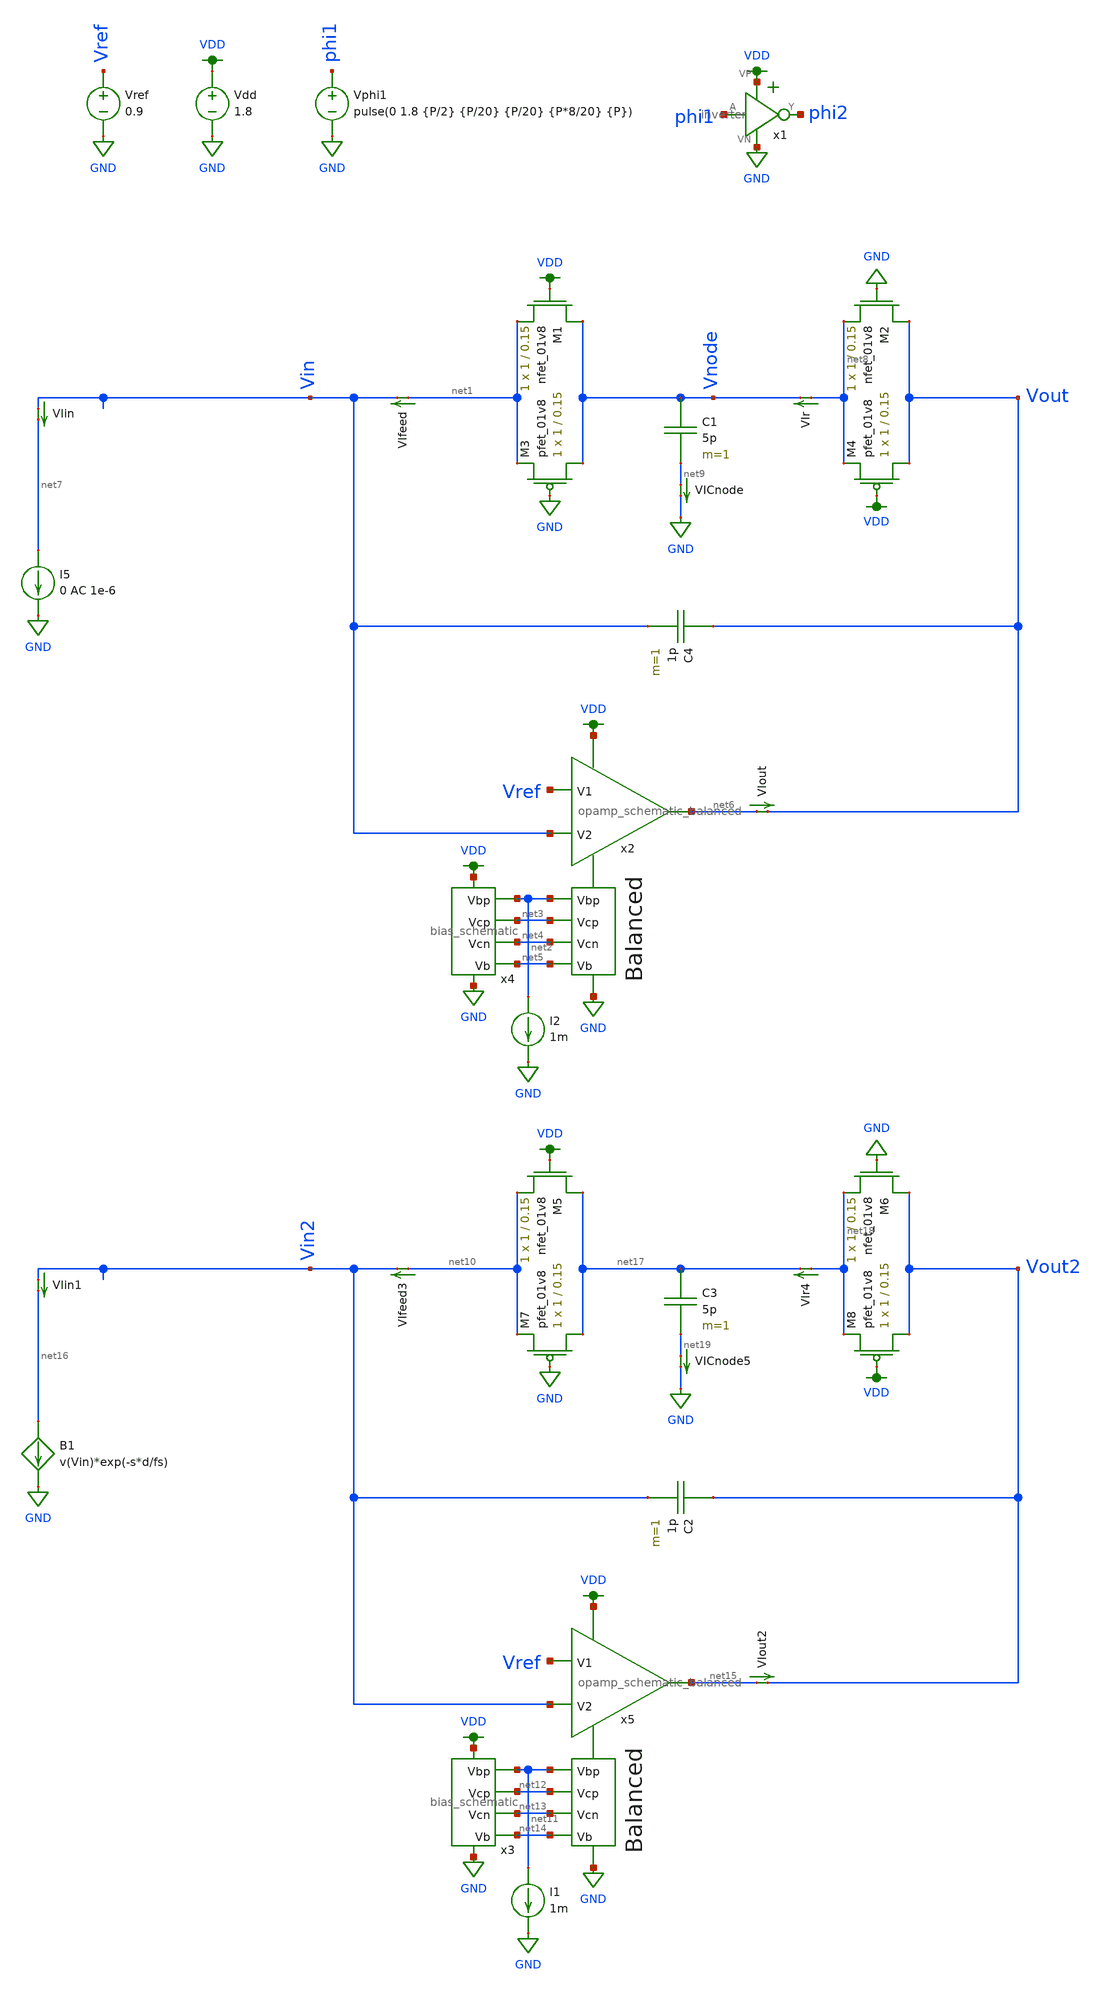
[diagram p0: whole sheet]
** sch_path: xschem/switched_capacitor/switched_capacitor_iv_bode_2_part.sch
**.subckt switched_capacitor_iv_bode_2_part
Vdd VDD GND 1.8
x4 VDD net2 net3 net4 GND net5 bias_schematic
Vref Vref GND 0.9
I2 net2 GND 1m
VIin Vin net7 0
.save i(viin)
VIout net6 Vout 0
.save i(viout)
VIfeed net1 Vin 0
.save i(vifeed)
C4 Vout Vin 1p m=1
x2 VDD net2 net3 net6 Vref Vin net4 net5 GND opamp_schematic_balanced
I5 net7 GND 0 AC 1e-6
C1 Vnode net9 5p m=1
XM1 Vnode VDD net1 GND sky130_fd_pr__nfet_01v8 L=0.15 W=1 nf=1 ad='int((nf+1)/2) * W/nf * 0.29' as='int((nf+2)/2) * W/nf * 0.29'
+ pd='2*int((nf+1)/2) * (W/nf + 0.29)' ps='2*int((nf+2)/2) * (W/nf + 0.29)' nrd='0.29 / W' nrs='0.29 / W'
+ sa=0 sb=0 sd=0 mult=1 m=1
XM2 Vout GND net8 GND sky130_fd_pr__nfet_01v8 L=0.15 W=1 nf=1 ad='int((nf+1)/2) * W/nf * 0.29' as='int((nf+2)/2) * W/nf * 0.29'
+ pd='2*int((nf+1)/2) * (W/nf + 0.29)' ps='2*int((nf+2)/2) * (W/nf + 0.29)' nrd='0.29 / W' nrs='0.29 / W'
+ sa=0 sb=0 sd=0 mult=1 m=1
XM3 Vnode GND net1 VDD sky130_fd_pr__pfet_01v8 L=0.15 W=1 nf=1 ad='int((nf+1)/2) * W/nf * 0.29' as='int((nf+2)/2) * W/nf * 0.29'
+ pd='2*int((nf+1)/2) * (W/nf + 0.29)' ps='2*int((nf+2)/2) * (W/nf + 0.29)' nrd='0.29 / W' nrs='0.29 / W'
+ sa=0 sb=0 sd=0 mult=1 m=1
XM4 Vout VDD net8 VDD sky130_fd_pr__pfet_01v8 L=0.15 W=1 nf=1 ad='int((nf+1)/2) * W/nf * 0.29' as='int((nf+2)/2) * W/nf * 0.29'
+ pd='2*int((nf+1)/2) * (W/nf + 0.29)' ps='2*int((nf+2)/2) * (W/nf + 0.29)' nrd='0.29 / W' nrs='0.29 / W'
+ sa=0 sb=0 sd=0 mult=1 m=1
x1 VDD phi1 phi2 GND inverter
VIr net8 Vnode 0
.save i(vir)
VICnode net9 GND 0
.save i(vicnode)
Vphi1 phi1 GND pulse(0 1.8 {P/2} {P/20} {P/20} {P*8/20} {P})
x3 VDD net11 net12 net13 GND net14 bias_schematic
I1 net11 GND 1m
VIin1 Vin2 net16 0
.save i(viin1)
VIout2 net15 Vout2 0
.save i(viout2)
VIfeed3 net10 Vin2 0
.save i(vifeed3)
C2 Vout2 Vin2 1p m=1
x5 VDD net11 net12 net15 Vref Vin2 net13 net14 GND opamp_schematic_balanced
C3 net17 net19 5p m=1
XM5 net17 VDD net10 GND sky130_fd_pr__nfet_01v8 L=0.15 W=1 nf=1 ad='int((nf+1)/2) * W/nf * 0.29' as='int((nf+2)/2) * W/nf * 0.29'
+ pd='2*int((nf+1)/2) * (W/nf + 0.29)' ps='2*int((nf+2)/2) * (W/nf + 0.29)' nrd='0.29 / W' nrs='0.29 / W'
+ sa=0 sb=0 sd=0 mult=1 m=1
XM6 Vout2 GND net18 GND sky130_fd_pr__nfet_01v8 L=0.15 W=1 nf=1 ad='int((nf+1)/2) * W/nf * 0.29' as='int((nf+2)/2) * W/nf * 0.29'
+ pd='2*int((nf+1)/2) * (W/nf + 0.29)' ps='2*int((nf+2)/2) * (W/nf + 0.29)' nrd='0.29 / W' nrs='0.29 / W'
+ sa=0 sb=0 sd=0 mult=1 m=1
XM7 net17 GND net10 VDD sky130_fd_pr__pfet_01v8 L=0.15 W=1 nf=1 ad='int((nf+1)/2) * W/nf * 0.29' as='int((nf+2)/2) * W/nf * 0.29'
+ pd='2*int((nf+1)/2) * (W/nf + 0.29)' ps='2*int((nf+2)/2) * (W/nf + 0.29)' nrd='0.29 / W' nrs='0.29 / W'
+ sa=0 sb=0 sd=0 mult=1 m=1
XM8 Vout2 VDD net18 VDD sky130_fd_pr__pfet_01v8 L=0.15 W=1 nf=1 ad='int((nf+1)/2) * W/nf * 0.29' as='int((nf+2)/2) * W/nf * 0.29'
+ pd='2*int((nf+1)/2) * (W/nf + 0.29)' ps='2*int((nf+2)/2) * (W/nf + 0.29)' nrd='0.29 / W' nrs='0.29 / W'
+ sa=0 sb=0 sd=0 mult=1 m=1
VIr4 net18 net17 0
.save i(vir4)
VICnode5 net19 GND 0
.save i(vicnode5)
B1 net16 GND I=v(Vin)*exp(-s*d/fs)
**** begin user architecture code

.option wnflag=1
.param MC_SWITCH=0.0
.lib ~/skywater/skywater-pdk/libraries/sky130_fd_pr_ngspice/latest/models/sky130.lib.spice tt


.param P=10n
.pss 5e-6 Vout 1024 50
.param fs=100Meg d=0.5
ac dec 1e2 1 1e10
*.control
*save all
*ac dec 1e-1 1 1e10
*run
*plot db(v(Vout)) cph(v(Vout))*180/pi
*.endc

**** end user architecture code
**.ends

* expanding   symbol:  /home/madvlsi/dev/git/magic-dds/xschem/other_project_files/bias_schematic.sym
*+ # of pins=6
** sym_path: xschem/other_project_files/bias_schematic.sym
** sch_path: xschem/other_project_files/bias_schematic.sch
.subckt bias_schematic VP Vbp Vcp Vcn VN Vb
*.iopin VP
*.iopin VN
*.opin Vcp
*.iopin Vbp
*.opin Vcn
*.opin Vb
XM1a net2 net2 net1 GND sky130_fd_pr__nfet_01v8 L=0.5 W=3 nf=1 ad='int((nf+1)/2) * W/nf * 0.29' as='int((nf+2)/2) * W/nf * 0.29'
+ pd='2*int((nf+1)/2) * (W/nf + 0.29)' ps='2*int((nf+2)/2) * (W/nf + 0.29)' nrd='0.29 / W' nrs='0.29 / W'
+ sa=0 sb=0 sd=0 mult=1 m=1
XM1b net2 net2 net1 GND sky130_fd_pr__nfet_01v8 L=0.5 W=3 nf=1 ad='int((nf+1)/2) * W/nf * 0.29' as='int((nf+2)/2) * W/nf * 0.29'
+ pd='2*int((nf+1)/2) * (W/nf + 0.29)' ps='2*int((nf+2)/2) * (W/nf + 0.29)' nrd='0.29 / W' nrs='0.29 / W'
+ sa=0 sb=0 sd=0 mult=1 m=1
XM1c net2 net2 net1 GND sky130_fd_pr__nfet_01v8 L=0.5 W=3 nf=1 ad='int((nf+1)/2) * W/nf * 0.29' as='int((nf+2)/2) * W/nf * 0.29'
+ pd='2*int((nf+1)/2) * (W/nf + 0.29)' ps='2*int((nf+2)/2) * (W/nf + 0.29)' nrd='0.29 / W' nrs='0.29 / W'
+ sa=0 sb=0 sd=0 mult=1 m=1
XM1d net2 net2 net1 GND sky130_fd_pr__nfet_01v8 L=0.5 W=3 nf=1 ad='int((nf+1)/2) * W/nf * 0.29' as='int((nf+2)/2) * W/nf * 0.29'
+ pd='2*int((nf+1)/2) * (W/nf + 0.29)' ps='2*int((nf+2)/2) * (W/nf + 0.29)' nrd='0.29 / W' nrs='0.29 / W'
+ sa=0 sb=0 sd=0 mult=1 m=1
XM2a VN net2 net1 GND sky130_fd_pr__nfet_01v8 L=0.5 W=3 nf=1 ad='int((nf+1)/2) * W/nf * 0.29' as='int((nf+2)/2) * W/nf * 0.29'
+ pd='2*int((nf+1)/2) * (W/nf + 0.29)' ps='2*int((nf+2)/2) * (W/nf + 0.29)' nrd='0.29 / W' nrs='0.29 / W'
+ sa=0 sb=0 sd=0 mult=1 m=1
XM2b VN net2 net1 GND sky130_fd_pr__nfet_01v8 L=0.5 W=3 nf=1 ad='int((nf+1)/2) * W/nf * 0.29' as='int((nf+2)/2) * W/nf * 0.29'
+ pd='2*int((nf+1)/2) * (W/nf + 0.29)' ps='2*int((nf+2)/2) * (W/nf + 0.29)' nrd='0.29 / W' nrs='0.29 / W'
+ sa=0 sb=0 sd=0 mult=1 m=1
XM2c VN net2 net1 GND sky130_fd_pr__nfet_01v8 L=0.5 W=3 nf=1 ad='int((nf+1)/2) * W/nf * 0.29' as='int((nf+2)/2) * W/nf * 0.29'
+ pd='2*int((nf+1)/2) * (W/nf + 0.29)' ps='2*int((nf+2)/2) * (W/nf + 0.29)' nrd='0.29 / W' nrs='0.29 / W'
+ sa=0 sb=0 sd=0 mult=1 m=1
XM2d VN net2 net1 GND sky130_fd_pr__nfet_01v8 L=0.5 W=3 nf=1 ad='int((nf+1)/2) * W/nf * 0.29' as='int((nf+2)/2) * W/nf * 0.29'
+ pd='2*int((nf+1)/2) * (W/nf + 0.29)' ps='2*int((nf+2)/2) * (W/nf + 0.29)' nrd='0.29 / W' nrs='0.29 / W'
+ sa=0 sb=0 sd=0 mult=1 m=1
XM3a net2 Vbp net7 VDD sky130_fd_pr__pfet_01v8 L=0.5 W=3 nf=1 ad='int((nf+1)/2) * W/nf * 0.29' as='int((nf+2)/2) * W/nf * 0.29'
+ pd='2*int((nf+1)/2) * (W/nf + 0.29)' ps='2*int((nf+2)/2) * (W/nf + 0.29)' nrd='0.29 / W' nrs='0.29 / W'
+ sa=0 sb=0 sd=0 mult=1 m=1
XM3b net7 Vbp net6 VDD sky130_fd_pr__pfet_01v8 L=0.5 W=3 nf=1 ad='int((nf+1)/2) * W/nf * 0.29' as='int((nf+2)/2) * W/nf * 0.29'
+ pd='2*int((nf+1)/2) * (W/nf + 0.29)' ps='2*int((nf+2)/2) * (W/nf + 0.29)' nrd='0.29 / W' nrs='0.29 / W'
+ sa=0 sb=0 sd=0 mult=1 m=1
XM3c net6 Vbp net5 VDD sky130_fd_pr__pfet_01v8 L=0.5 W=3 nf=1 ad='int((nf+1)/2) * W/nf * 0.29' as='int((nf+2)/2) * W/nf * 0.29'
+ pd='2*int((nf+1)/2) * (W/nf + 0.29)' ps='2*int((nf+2)/2) * (W/nf + 0.29)' nrd='0.29 / W' nrs='0.29 / W'
+ sa=0 sb=0 sd=0 mult=1 m=1
XM3d net5 Vbp VP VDD sky130_fd_pr__pfet_01v8 L=0.5 W=3 nf=1 ad='int((nf+1)/2) * W/nf * 0.29' as='int((nf+2)/2) * W/nf * 0.29'
+ pd='2*int((nf+1)/2) * (W/nf + 0.29)' ps='2*int((nf+2)/2) * (W/nf + 0.29)' nrd='0.29 / W' nrs='0.29 / W'
+ sa=0 sb=0 sd=0 mult=1 m=1
XM4a Vcn Vbp VP VDD sky130_fd_pr__pfet_01v8 L=0.5 W=3 nf=1 ad='int((nf+1)/2) * W/nf * 0.29' as='int((nf+2)/2) * W/nf * 0.29'
+ pd='2*int((nf+1)/2) * (W/nf + 0.29)' ps='2*int((nf+2)/2) * (W/nf + 0.29)' nrd='0.29 / W' nrs='0.29 / W'
+ sa=0 sb=0 sd=0 mult=1 m=1
XM4b Vcn Vbp VP VDD sky130_fd_pr__pfet_01v8 L=0.5 W=3 nf=1 ad='int((nf+1)/2) * W/nf * 0.29' as='int((nf+2)/2) * W/nf * 0.29'
+ pd='2*int((nf+1)/2) * (W/nf + 0.29)' ps='2*int((nf+2)/2) * (W/nf + 0.29)' nrd='0.29 / W' nrs='0.29 / W'
+ sa=0 sb=0 sd=0 mult=1 m=1
XM4c Vcn Vbp VP VDD sky130_fd_pr__pfet_01v8 L=0.5 W=3 nf=1 ad='int((nf+1)/2) * W/nf * 0.29' as='int((nf+2)/2) * W/nf * 0.29'
+ pd='2*int((nf+1)/2) * (W/nf + 0.29)' ps='2*int((nf+2)/2) * (W/nf + 0.29)' nrd='0.29 / W' nrs='0.29 / W'
+ sa=0 sb=0 sd=0 mult=1 m=1
XM4d Vcn Vbp VP VDD sky130_fd_pr__pfet_01v8 L=0.5 W=3 nf=1 ad='int((nf+1)/2) * W/nf * 0.29' as='int((nf+2)/2) * W/nf * 0.29'
+ pd='2*int((nf+1)/2) * (W/nf + 0.29)' ps='2*int((nf+2)/2) * (W/nf + 0.29)' nrd='0.29 / W' nrs='0.29 / W'
+ sa=0 sb=0 sd=0 mult=1 m=1
XM11a VP Vbp Vbp VDD sky130_fd_pr__pfet_01v8 L=0.5 W=3 nf=1 ad='int((nf+1)/2) * W/nf * 0.29' as='int((nf+2)/2) * W/nf * 0.29'
+ pd='2*int((nf+1)/2) * (W/nf + 0.29)' ps='2*int((nf+2)/2) * (W/nf + 0.29)' nrd='0.29 / W' nrs='0.29 / W'
+ sa=0 sb=0 sd=0 mult=1 m=1
XM11b VP Vbp Vbp VDD sky130_fd_pr__pfet_01v8 L=0.5 W=3 nf=1 ad='int((nf+1)/2) * W/nf * 0.29' as='int((nf+2)/2) * W/nf * 0.29'
+ pd='2*int((nf+1)/2) * (W/nf + 0.29)' ps='2*int((nf+2)/2) * (W/nf + 0.29)' nrd='0.29 / W' nrs='0.29 / W'
+ sa=0 sb=0 sd=0 mult=1 m=1
XM11c VP Vbp Vbp VDD sky130_fd_pr__pfet_01v8 L=0.5 W=3 nf=1 ad='int((nf+1)/2) * W/nf * 0.29' as='int((nf+2)/2) * W/nf * 0.29'
+ pd='2*int((nf+1)/2) * (W/nf + 0.29)' ps='2*int((nf+2)/2) * (W/nf + 0.29)' nrd='0.29 / W' nrs='0.29 / W'
+ sa=0 sb=0 sd=0 mult=1 m=1
XM11d VP Vbp Vbp VDD sky130_fd_pr__pfet_01v8 L=0.5 W=3 nf=1 ad='int((nf+1)/2) * W/nf * 0.29' as='int((nf+2)/2) * W/nf * 0.29'
+ pd='2*int((nf+1)/2) * (W/nf + 0.29)' ps='2*int((nf+2)/2) * (W/nf + 0.29)' nrd='0.29 / W' nrs='0.29 / W'
+ sa=0 sb=0 sd=0 mult=1 m=1
XM5a net1 Vcn Vcn GND sky130_fd_pr__nfet_01v8 L=0.5 W=3 nf=1 ad='int((nf+1)/2) * W/nf * 0.29' as='int((nf+2)/2) * W/nf * 0.29'
+ pd='2*int((nf+1)/2) * (W/nf + 0.29)' ps='2*int((nf+2)/2) * (W/nf + 0.29)' nrd='0.29 / W' nrs='0.29 / W'
+ sa=0 sb=0 sd=0 mult=1 m=1
XM5b net1 Vcn Vcn GND sky130_fd_pr__nfet_01v8 L=0.5 W=3 nf=1 ad='int((nf+1)/2) * W/nf * 0.29' as='int((nf+2)/2) * W/nf * 0.29'
+ pd='2*int((nf+1)/2) * (W/nf + 0.29)' ps='2*int((nf+2)/2) * (W/nf + 0.29)' nrd='0.29 / W' nrs='0.29 / W'
+ sa=0 sb=0 sd=0 mult=1 m=1
XM5c net1 Vcn Vcn GND sky130_fd_pr__nfet_01v8 L=0.5 W=3 nf=1 ad='int((nf+1)/2) * W/nf * 0.29' as='int((nf+2)/2) * W/nf * 0.29'
+ pd='2*int((nf+1)/2) * (W/nf + 0.29)' ps='2*int((nf+2)/2) * (W/nf + 0.29)' nrd='0.29 / W' nrs='0.29 / W'
+ sa=0 sb=0 sd=0 mult=1 m=1
XM5d net1 Vcn Vcn GND sky130_fd_pr__nfet_01v8 L=0.5 W=3 nf=1 ad='int((nf+1)/2) * W/nf * 0.29' as='int((nf+2)/2) * W/nf * 0.29'
+ pd='2*int((nf+1)/2) * (W/nf + 0.29)' ps='2*int((nf+2)/2) * (W/nf + 0.29)' nrd='0.29 / W' nrs='0.29 / W'
+ sa=0 sb=0 sd=0 mult=1 m=1
XM8a net10 Vb net3 GND sky130_fd_pr__nfet_01v8 L=0.5 W=3 nf=1 ad='int((nf+1)/2) * W/nf * 0.29' as='int((nf+2)/2) * W/nf * 0.29'
+ pd='2*int((nf+1)/2) * (W/nf + 0.29)' ps='2*int((nf+2)/2) * (W/nf + 0.29)' nrd='0.29 / W' nrs='0.29 / W'
+ sa=0 sb=0 sd=0 mult=1 m=1
XM8b net9 Vb net10 GND sky130_fd_pr__nfet_01v8 L=0.5 W=3 nf=1 ad='int((nf+1)/2) * W/nf * 0.29' as='int((nf+2)/2) * W/nf * 0.29'
+ pd='2*int((nf+1)/2) * (W/nf + 0.29)' ps='2*int((nf+2)/2) * (W/nf + 0.29)' nrd='0.29 / W' nrs='0.29 / W'
+ sa=0 sb=0 sd=0 mult=1 m=1
XM8c net8 Vb net9 GND sky130_fd_pr__nfet_01v8 L=0.5 W=3 nf=1 ad='int((nf+1)/2) * W/nf * 0.29' as='int((nf+2)/2) * W/nf * 0.29'
+ pd='2*int((nf+1)/2) * (W/nf + 0.29)' ps='2*int((nf+2)/2) * (W/nf + 0.29)' nrd='0.29 / W' nrs='0.29 / W'
+ sa=0 sb=0 sd=0 mult=1 m=1
XM8d VN Vb net8 GND sky130_fd_pr__nfet_01v8 L=0.5 W=3 nf=1 ad='int((nf+1)/2) * W/nf * 0.29' as='int((nf+2)/2) * W/nf * 0.29'
+ pd='2*int((nf+1)/2) * (W/nf + 0.29)' ps='2*int((nf+2)/2) * (W/nf + 0.29)' nrd='0.29 / W' nrs='0.29 / W'
+ sa=0 sb=0 sd=0 mult=1 m=1
XM6a net3 net3 net4 VDD sky130_fd_pr__pfet_01v8 L=0.5 W=3 nf=1 ad='int((nf+1)/2) * W/nf * 0.29' as='int((nf+2)/2) * W/nf * 0.29'
+ pd='2*int((nf+1)/2) * (W/nf + 0.29)' ps='2*int((nf+2)/2) * (W/nf + 0.29)' nrd='0.29 / W' nrs='0.29 / W'
+ sa=0 sb=0 sd=0 mult=1 m=1
XM6b net3 net3 net4 VDD sky130_fd_pr__pfet_01v8 L=0.5 W=3 nf=1 ad='int((nf+1)/2) * W/nf * 0.29' as='int((nf+2)/2) * W/nf * 0.29'
+ pd='2*int((nf+1)/2) * (W/nf + 0.29)' ps='2*int((nf+2)/2) * (W/nf + 0.29)' nrd='0.29 / W' nrs='0.29 / W'
+ sa=0 sb=0 sd=0 mult=1 m=1
XM6c net3 net3 net4 VDD sky130_fd_pr__pfet_01v8 L=0.5 W=3 nf=1 ad='int((nf+1)/2) * W/nf * 0.29' as='int((nf+2)/2) * W/nf * 0.29'
+ pd='2*int((nf+1)/2) * (W/nf + 0.29)' ps='2*int((nf+2)/2) * (W/nf + 0.29)' nrd='0.29 / W' nrs='0.29 / W'
+ sa=0 sb=0 sd=0 mult=1 m=1
XM6d net3 net3 net4 VDD sky130_fd_pr__pfet_01v8 L=0.5 W=3 nf=1 ad='int((nf+1)/2) * W/nf * 0.29' as='int((nf+2)/2) * W/nf * 0.29'
+ pd='2*int((nf+1)/2) * (W/nf + 0.29)' ps='2*int((nf+2)/2) * (W/nf + 0.29)' nrd='0.29 / W' nrs='0.29 / W'
+ sa=0 sb=0 sd=0 mult=1 m=1
XM7a net4 net3 VP VDD sky130_fd_pr__pfet_01v8 L=0.5 W=3 nf=1 ad='int((nf+1)/2) * W/nf * 0.29' as='int((nf+2)/2) * W/nf * 0.29'
+ pd='2*int((nf+1)/2) * (W/nf + 0.29)' ps='2*int((nf+2)/2) * (W/nf + 0.29)' nrd='0.29 / W' nrs='0.29 / W'
+ sa=0 sb=0 sd=0 mult=1 m=1
XM7b net4 net3 VP VDD sky130_fd_pr__pfet_01v8 L=0.5 W=3 nf=1 ad='int((nf+1)/2) * W/nf * 0.29' as='int((nf+2)/2) * W/nf * 0.29'
+ pd='2*int((nf+1)/2) * (W/nf + 0.29)' ps='2*int((nf+2)/2) * (W/nf + 0.29)' nrd='0.29 / W' nrs='0.29 / W'
+ sa=0 sb=0 sd=0 mult=1 m=1
XM7c net4 net3 VP VDD sky130_fd_pr__pfet_01v8 L=0.5 W=3 nf=1 ad='int((nf+1)/2) * W/nf * 0.29' as='int((nf+2)/2) * W/nf * 0.29'
+ pd='2*int((nf+1)/2) * (W/nf + 0.29)' ps='2*int((nf+2)/2) * (W/nf + 0.29)' nrd='0.29 / W' nrs='0.29 / W'
+ sa=0 sb=0 sd=0 mult=1 m=1
XM7d net4 net3 VP VDD sky130_fd_pr__pfet_01v8 L=0.5 W=3 nf=1 ad='int((nf+1)/2) * W/nf * 0.29' as='int((nf+2)/2) * W/nf * 0.29'
+ pd='2*int((nf+1)/2) * (W/nf + 0.29)' ps='2*int((nf+2)/2) * (W/nf + 0.29)' nrd='0.29 / W' nrs='0.29 / W'
+ sa=0 sb=0 sd=0 mult=1 m=1
XM10d net4 Vcp Vcp VDD sky130_fd_pr__pfet_01v8 L=0.5 W=3 nf=1 ad='int((nf+1)/2) * W/nf * 0.29' as='int((nf+2)/2) * W/nf * 0.29'
+ pd='2*int((nf+1)/2) * (W/nf + 0.29)' ps='2*int((nf+2)/2) * (W/nf + 0.29)' nrd='0.29 / W' nrs='0.29 / W'
+ sa=0 sb=0 sd=0 mult=1 m=1
XM10c net4 Vcp Vcp VDD sky130_fd_pr__pfet_01v8 L=0.5 W=3 nf=1 ad='int((nf+1)/2) * W/nf * 0.29' as='int((nf+2)/2) * W/nf * 0.29'
+ pd='2*int((nf+1)/2) * (W/nf + 0.29)' ps='2*int((nf+2)/2) * (W/nf + 0.29)' nrd='0.29 / W' nrs='0.29 / W'
+ sa=0 sb=0 sd=0 mult=1 m=1
XM10b net4 Vcp Vcp VDD sky130_fd_pr__pfet_01v8 L=0.5 W=3 nf=1 ad='int((nf+1)/2) * W/nf * 0.29' as='int((nf+2)/2) * W/nf * 0.29'
+ pd='2*int((nf+1)/2) * (W/nf + 0.29)' ps='2*int((nf+2)/2) * (W/nf + 0.29)' nrd='0.29 / W' nrs='0.29 / W'
+ sa=0 sb=0 sd=0 mult=1 m=1
XM10a net4 Vcp Vcp VDD sky130_fd_pr__pfet_01v8 L=0.5 W=3 nf=1 ad='int((nf+1)/2) * W/nf * 0.29' as='int((nf+2)/2) * W/nf * 0.29'
+ pd='2*int((nf+1)/2) * (W/nf + 0.29)' ps='2*int((nf+2)/2) * (W/nf + 0.29)' nrd='0.29 / W' nrs='0.29 / W'
+ sa=0 sb=0 sd=0 mult=1 m=1
XM9a VN Vb Vcp GND sky130_fd_pr__nfet_01v8 L=0.5 W=3 nf=1 ad='int((nf+1)/2) * W/nf * 0.29' as='int((nf+2)/2) * W/nf * 0.29'
+ pd='2*int((nf+1)/2) * (W/nf + 0.29)' ps='2*int((nf+2)/2) * (W/nf + 0.29)' nrd='0.29 / W' nrs='0.29 / W'
+ sa=0 sb=0 sd=0 mult=1 m=1
XM9b VN Vb Vcp GND sky130_fd_pr__nfet_01v8 L=0.5 W=3 nf=1 ad='int((nf+1)/2) * W/nf * 0.29' as='int((nf+2)/2) * W/nf * 0.29'
+ pd='2*int((nf+1)/2) * (W/nf + 0.29)' ps='2*int((nf+2)/2) * (W/nf + 0.29)' nrd='0.29 / W' nrs='0.29 / W'
+ sa=0 sb=0 sd=0 mult=1 m=1
XM9c VN Vb Vcp GND sky130_fd_pr__nfet_01v8 L=0.5 W=3 nf=1 ad='int((nf+1)/2) * W/nf * 0.29' as='int((nf+2)/2) * W/nf * 0.29'
+ pd='2*int((nf+1)/2) * (W/nf + 0.29)' ps='2*int((nf+2)/2) * (W/nf + 0.29)' nrd='0.29 / W' nrs='0.29 / W'
+ sa=0 sb=0 sd=0 mult=1 m=1
XM9d VN Vb Vcp GND sky130_fd_pr__nfet_01v8 L=0.5 W=3 nf=1 ad='int((nf+1)/2) * W/nf * 0.29' as='int((nf+2)/2) * W/nf * 0.29'
+ pd='2*int((nf+1)/2) * (W/nf + 0.29)' ps='2*int((nf+2)/2) * (W/nf + 0.29)' nrd='0.29 / W' nrs='0.29 / W'
+ sa=0 sb=0 sd=0 mult=1 m=1
XM12a VN Vb Vb GND sky130_fd_pr__nfet_01v8 L=0.5 W=3 nf=1 ad='int((nf+1)/2) * W/nf * 0.29' as='int((nf+2)/2) * W/nf * 0.29'
+ pd='2*int((nf+1)/2) * (W/nf + 0.29)' ps='2*int((nf+2)/2) * (W/nf + 0.29)' nrd='0.29 / W' nrs='0.29 / W'
+ sa=0 sb=0 sd=0 mult=1 m=1
XM12b VN Vb Vb GND sky130_fd_pr__nfet_01v8 L=0.5 W=3 nf=1 ad='int((nf+1)/2) * W/nf * 0.29' as='int((nf+2)/2) * W/nf * 0.29'
+ pd='2*int((nf+1)/2) * (W/nf + 0.29)' ps='2*int((nf+2)/2) * (W/nf + 0.29)' nrd='0.29 / W' nrs='0.29 / W'
+ sa=0 sb=0 sd=0 mult=1 m=1
XM12c VN Vb Vb GND sky130_fd_pr__nfet_01v8 L=0.5 W=3 nf=1 ad='int((nf+1)/2) * W/nf * 0.29' as='int((nf+2)/2) * W/nf * 0.29'
+ pd='2*int((nf+1)/2) * (W/nf + 0.29)' ps='2*int((nf+2)/2) * (W/nf + 0.29)' nrd='0.29 / W' nrs='0.29 / W'
+ sa=0 sb=0 sd=0 mult=1 m=1
XM12d VN Vb Vb GND sky130_fd_pr__nfet_01v8 L=0.5 W=3 nf=1 ad='int((nf+1)/2) * W/nf * 0.29' as='int((nf+2)/2) * W/nf * 0.29'
+ pd='2*int((nf+1)/2) * (W/nf + 0.29)' ps='2*int((nf+2)/2) * (W/nf + 0.29)' nrd='0.29 / W' nrs='0.29 / W'
+ sa=0 sb=0 sd=0 mult=1 m=1
XM1 Vb Vbp VP VDD sky130_fd_pr__pfet_01v8 L=0.5 W=3 nf=1 ad='int((nf+1)/2) * W/nf * 0.29' as='int((nf+2)/2) * W/nf * 0.29'
+ pd='2*int((nf+1)/2) * (W/nf + 0.29)' ps='2*int((nf+2)/2) * (W/nf + 0.29)' nrd='0.29 / W' nrs='0.29 / W'
+ sa=0 sb=0 sd=0 mult=1 m=1
XM2 Vb Vbp VP VDD sky130_fd_pr__pfet_01v8 L=0.5 W=3 nf=1 ad='int((nf+1)/2) * W/nf * 0.29' as='int((nf+2)/2) * W/nf * 0.29'
+ pd='2*int((nf+1)/2) * (W/nf + 0.29)' ps='2*int((nf+2)/2) * (W/nf + 0.29)' nrd='0.29 / W' nrs='0.29 / W'
+ sa=0 sb=0 sd=0 mult=1 m=1
XM3 Vb Vbp VP VDD sky130_fd_pr__pfet_01v8 L=0.5 W=3 nf=1 ad='int((nf+1)/2) * W/nf * 0.29' as='int((nf+2)/2) * W/nf * 0.29'
+ pd='2*int((nf+1)/2) * (W/nf + 0.29)' ps='2*int((nf+2)/2) * (W/nf + 0.29)' nrd='0.29 / W' nrs='0.29 / W'
+ sa=0 sb=0 sd=0 mult=1 m=1
XM4 Vb Vbp VP VDD sky130_fd_pr__pfet_01v8 L=0.5 W=3 nf=1 ad='int((nf+1)/2) * W/nf * 0.29' as='int((nf+2)/2) * W/nf * 0.29'
+ pd='2*int((nf+1)/2) * (W/nf + 0.29)' ps='2*int((nf+2)/2) * (W/nf + 0.29)' nrd='0.29 / W' nrs='0.29 / W'
+ sa=0 sb=0 sd=0 mult=1 m=1
XM1e net2 net2 net1 GND sky130_fd_pr__nfet_01v8 L=0.5 W=3 nf=1 ad='int((nf+1)/2) * W/nf * 0.29' as='int((nf+2)/2) * W/nf * 0.29'
+ pd='2*int((nf+1)/2) * (W/nf + 0.29)' ps='2*int((nf+2)/2) * (W/nf + 0.29)' nrd='0.29 / W' nrs='0.29 / W'
+ sa=0 sb=0 sd=0 mult=1 m=1
XM1f net2 net2 net1 GND sky130_fd_pr__nfet_01v8 L=0.5 W=3 nf=1 ad='int((nf+1)/2) * W/nf * 0.29' as='int((nf+2)/2) * W/nf * 0.29'
+ pd='2*int((nf+1)/2) * (W/nf + 0.29)' ps='2*int((nf+2)/2) * (W/nf + 0.29)' nrd='0.29 / W' nrs='0.29 / W'
+ sa=0 sb=0 sd=0 mult=1 m=1
XM1g net2 net2 net1 GND sky130_fd_pr__nfet_01v8 L=0.5 W=3 nf=1 ad='int((nf+1)/2) * W/nf * 0.29' as='int((nf+2)/2) * W/nf * 0.29'
+ pd='2*int((nf+1)/2) * (W/nf + 0.29)' ps='2*int((nf+2)/2) * (W/nf + 0.29)' nrd='0.29 / W' nrs='0.29 / W'
+ sa=0 sb=0 sd=0 mult=1 m=1
XM1h net2 net2 net1 GND sky130_fd_pr__nfet_01v8 L=0.5 W=3 nf=1 ad='int((nf+1)/2) * W/nf * 0.29' as='int((nf+2)/2) * W/nf * 0.29'
+ pd='2*int((nf+1)/2) * (W/nf + 0.29)' ps='2*int((nf+2)/2) * (W/nf + 0.29)' nrd='0.29 / W' nrs='0.29 / W'
+ sa=0 sb=0 sd=0 mult=1 m=1
XM6e net3 net3 net4 VDD sky130_fd_pr__pfet_01v8 L=0.5 W=3 nf=1 ad='int((nf+1)/2) * W/nf * 0.29' as='int((nf+2)/2) * W/nf * 0.29'
+ pd='2*int((nf+1)/2) * (W/nf + 0.29)' ps='2*int((nf+2)/2) * (W/nf + 0.29)' nrd='0.29 / W' nrs='0.29 / W'
+ sa=0 sb=0 sd=0 mult=1 m=1
XM6f net3 net3 net4 VDD sky130_fd_pr__pfet_01v8 L=0.5 W=3 nf=1 ad='int((nf+1)/2) * W/nf * 0.29' as='int((nf+2)/2) * W/nf * 0.29'
+ pd='2*int((nf+1)/2) * (W/nf + 0.29)' ps='2*int((nf+2)/2) * (W/nf + 0.29)' nrd='0.29 / W' nrs='0.29 / W'
+ sa=0 sb=0 sd=0 mult=1 m=1
XM6g net3 net3 net4 VDD sky130_fd_pr__pfet_01v8 L=0.5 W=3 nf=1 ad='int((nf+1)/2) * W/nf * 0.29' as='int((nf+2)/2) * W/nf * 0.29'
+ pd='2*int((nf+1)/2) * (W/nf + 0.29)' ps='2*int((nf+2)/2) * (W/nf + 0.29)' nrd='0.29 / W' nrs='0.29 / W'
+ sa=0 sb=0 sd=0 mult=1 m=1
XM6h net3 net3 net4 VDD sky130_fd_pr__pfet_01v8 L=0.5 W=3 nf=1 ad='int((nf+1)/2) * W/nf * 0.29' as='int((nf+2)/2) * W/nf * 0.29'
+ pd='2*int((nf+1)/2) * (W/nf + 0.29)' ps='2*int((nf+2)/2) * (W/nf + 0.29)' nrd='0.29 / W' nrs='0.29 / W'
+ sa=0 sb=0 sd=0 mult=1 m=1
XM1i net2 net2 net1 GND sky130_fd_pr__nfet_01v8 L=0.5 W=3 nf=1 ad='int((nf+1)/2) * W/nf * 0.29' as='int((nf+2)/2) * W/nf * 0.29'
+ pd='2*int((nf+1)/2) * (W/nf + 0.29)' ps='2*int((nf+2)/2) * (W/nf + 0.29)' nrd='0.29 / W' nrs='0.29 / W'
+ sa=0 sb=0 sd=0 mult=1 m=1
XM1j net2 net2 net1 GND sky130_fd_pr__nfet_01v8 L=0.5 W=3 nf=1 ad='int((nf+1)/2) * W/nf * 0.29' as='int((nf+2)/2) * W/nf * 0.29'
+ pd='2*int((nf+1)/2) * (W/nf + 0.29)' ps='2*int((nf+2)/2) * (W/nf + 0.29)' nrd='0.29 / W' nrs='0.29 / W'
+ sa=0 sb=0 sd=0 mult=1 m=1
XM1k net2 net2 net1 GND sky130_fd_pr__nfet_01v8 L=0.5 W=3 nf=1 ad='int((nf+1)/2) * W/nf * 0.29' as='int((nf+2)/2) * W/nf * 0.29'
+ pd='2*int((nf+1)/2) * (W/nf + 0.29)' ps='2*int((nf+2)/2) * (W/nf + 0.29)' nrd='0.29 / W' nrs='0.29 / W'
+ sa=0 sb=0 sd=0 mult=1 m=1
XM1l net2 net2 net1 GND sky130_fd_pr__nfet_01v8 L=0.5 W=3 nf=1 ad='int((nf+1)/2) * W/nf * 0.29' as='int((nf+2)/2) * W/nf * 0.29'
+ pd='2*int((nf+1)/2) * (W/nf + 0.29)' ps='2*int((nf+2)/2) * (W/nf + 0.29)' nrd='0.29 / W' nrs='0.29 / W'
+ sa=0 sb=0 sd=0 mult=1 m=1
XM6i net3 net3 net4 VDD sky130_fd_pr__pfet_01v8 L=0.5 W=3 nf=1 ad='int((nf+1)/2) * W/nf * 0.29' as='int((nf+2)/2) * W/nf * 0.29'
+ pd='2*int((nf+1)/2) * (W/nf + 0.29)' ps='2*int((nf+2)/2) * (W/nf + 0.29)' nrd='0.29 / W' nrs='0.29 / W'
+ sa=0 sb=0 sd=0 mult=1 m=1
XM6j net3 net3 net4 VDD sky130_fd_pr__pfet_01v8 L=0.5 W=3 nf=1 ad='int((nf+1)/2) * W/nf * 0.29' as='int((nf+2)/2) * W/nf * 0.29'
+ pd='2*int((nf+1)/2) * (W/nf + 0.29)' ps='2*int((nf+2)/2) * (W/nf + 0.29)' nrd='0.29 / W' nrs='0.29 / W'
+ sa=0 sb=0 sd=0 mult=1 m=1
XM6k net3 net3 net4 VDD sky130_fd_pr__pfet_01v8 L=0.5 W=3 nf=1 ad='int((nf+1)/2) * W/nf * 0.29' as='int((nf+2)/2) * W/nf * 0.29'
+ pd='2*int((nf+1)/2) * (W/nf + 0.29)' ps='2*int((nf+2)/2) * (W/nf + 0.29)' nrd='0.29 / W' nrs='0.29 / W'
+ sa=0 sb=0 sd=0 mult=1 m=1
XM6l net3 net3 net4 VDD sky130_fd_pr__pfet_01v8 L=0.5 W=3 nf=1 ad='int((nf+1)/2) * W/nf * 0.29' as='int((nf+2)/2) * W/nf * 0.29'
+ pd='2*int((nf+1)/2) * (W/nf + 0.29)' ps='2*int((nf+2)/2) * (W/nf + 0.29)' nrd='0.29 / W' nrs='0.29 / W'
+ sa=0 sb=0 sd=0 mult=1 m=1
.ends


* expanding   symbol:
*+  /home/madvlsi/dev/git/magic-dds/xschem/other_project_files/opamp_schematic_balanced.sym # of pins=9
** sym_path: xschem/other_project_files/opamp_schematic_balanced.sym
** sch_path: xschem/other_project_files/opamp_schematic_balanced.sch
.subckt opamp_schematic_balanced VP Vbp Vcp Vout V1 V2 Vcn Vb VN
*.ipin Vbp
*.ipin Vcp
*.ipin Vcn
*.ipin V2
*.ipin V1
*.ipin Vb
*.iopin VP
*.iopin VN
*.opin Vout
XM1a M1top V1 Vnode GND sky130_fd_pr__nfet_01v8 L=0.5 W=3 nf=1 ad='int((nf+1)/2) * W/nf * 0.29' as='int((nf+2)/2) * W/nf * 0.29'
+ pd='2*int((nf+1)/2) * (W/nf + 0.29)' ps='2*int((nf+2)/2) * (W/nf + 0.29)' nrd='0.29 / W' nrs='0.29 / W'
+ sa=0 sb=0 sd=0 mult=1 m=1
XM1b M1top V1 Vnode GND sky130_fd_pr__nfet_01v8 L=0.5 W=3 nf=1 ad='int((nf+1)/2) * W/nf * 0.29' as='int((nf+2)/2) * W/nf * 0.29'
+ pd='2*int((nf+1)/2) * (W/nf + 0.29)' ps='2*int((nf+2)/2) * (W/nf + 0.29)' nrd='0.29 / W' nrs='0.29 / W'
+ sa=0 sb=0 sd=0 mult=1 m=1
XM1c M1top V1 Vnode GND sky130_fd_pr__nfet_01v8 L=0.5 W=3 nf=1 ad='int((nf+1)/2) * W/nf * 0.29' as='int((nf+2)/2) * W/nf * 0.29'
+ pd='2*int((nf+1)/2) * (W/nf + 0.29)' ps='2*int((nf+2)/2) * (W/nf + 0.29)' nrd='0.29 / W' nrs='0.29 / W'
+ sa=0 sb=0 sd=0 mult=1 m=1
XM1d M1top V1 Vnode GND sky130_fd_pr__nfet_01v8 L=0.5 W=3 nf=1 ad='int((nf+1)/2) * W/nf * 0.29' as='int((nf+2)/2) * W/nf * 0.29'
+ pd='2*int((nf+1)/2) * (W/nf + 0.29)' ps='2*int((nf+2)/2) * (W/nf + 0.29)' nrd='0.29 / W' nrs='0.29 / W'
+ sa=0 sb=0 sd=0 mult=1 m=1
XM2a M2top V2 Vnode GND sky130_fd_pr__nfet_01v8 L=0.5 W=3 nf=1 ad='int((nf+1)/2) * W/nf * 0.29' as='int((nf+2)/2) * W/nf * 0.29'
+ pd='2*int((nf+1)/2) * (W/nf + 0.29)' ps='2*int((nf+2)/2) * (W/nf + 0.29)' nrd='0.29 / W' nrs='0.29 / W'
+ sa=0 sb=0 sd=0 mult=1 m=1
XM2b M2top V2 Vnode GND sky130_fd_pr__nfet_01v8 L=0.5 W=3 nf=1 ad='int((nf+1)/2) * W/nf * 0.29' as='int((nf+2)/2) * W/nf * 0.29'
+ pd='2*int((nf+1)/2) * (W/nf + 0.29)' ps='2*int((nf+2)/2) * (W/nf + 0.29)' nrd='0.29 / W' nrs='0.29 / W'
+ sa=0 sb=0 sd=0 mult=1 m=1
XM2c M2top V2 Vnode GND sky130_fd_pr__nfet_01v8 L=0.5 W=3 nf=1 ad='int((nf+1)/2) * W/nf * 0.29' as='int((nf+2)/2) * W/nf * 0.29'
+ pd='2*int((nf+1)/2) * (W/nf + 0.29)' ps='2*int((nf+2)/2) * (W/nf + 0.29)' nrd='0.29 / W' nrs='0.29 / W'
+ sa=0 sb=0 sd=0 mult=1 m=1
XM2d M2top V2 Vnode GND sky130_fd_pr__nfet_01v8 L=0.5 W=3 nf=1 ad='int((nf+1)/2) * W/nf * 0.29' as='int((nf+2)/2) * W/nf * 0.29'
+ pd='2*int((nf+1)/2) * (W/nf + 0.29)' ps='2*int((nf+2)/2) * (W/nf + 0.29)' nrd='0.29 / W' nrs='0.29 / W'
+ sa=0 sb=0 sd=0 mult=1 m=1
XMba Vnode Vb VN GND sky130_fd_pr__nfet_01v8 L=0.5 W=1.5 nf=1 ad='int((nf+1)/2) * W/nf * 0.29' as='int((nf+2)/2) * W/nf * 0.29'
+ pd='2*int((nf+1)/2) * (W/nf + 0.29)' ps='2*int((nf+2)/2) * (W/nf + 0.29)' nrd='0.29 / W' nrs='0.29 / W'
+ sa=0 sb=0 sd=0 mult=1 m=1
XMbb Vnode Vb VN GND sky130_fd_pr__nfet_01v8 L=0.5 W=1.5 nf=1 ad='int((nf+1)/2) * W/nf * 0.29' as='int((nf+2)/2) * W/nf * 0.29'
+ pd='2*int((nf+1)/2) * (W/nf + 0.29)' ps='2*int((nf+2)/2) * (W/nf + 0.29)' nrd='0.29 / W' nrs='0.29 / W'
+ sa=0 sb=0 sd=0 mult=1 m=1
XMbc Vnode Vb VN GND sky130_fd_pr__nfet_01v8 L=0.5 W=1.5 nf=1 ad='int((nf+1)/2) * W/nf * 0.29' as='int((nf+2)/2) * W/nf * 0.29'
+ pd='2*int((nf+1)/2) * (W/nf + 0.29)' ps='2*int((nf+2)/2) * (W/nf + 0.29)' nrd='0.29 / W' nrs='0.29 / W'
+ sa=0 sb=0 sd=0 mult=1 m=1
XMbd Vnode Vb VN GND sky130_fd_pr__nfet_01v8 L=0.5 W=1.5 nf=1 ad='int((nf+1)/2) * W/nf * 0.29' as='int((nf+2)/2) * W/nf * 0.29'
+ pd='2*int((nf+1)/2) * (W/nf + 0.29)' ps='2*int((nf+2)/2) * (W/nf + 0.29)' nrd='0.29 / W' nrs='0.29 / W'
+ sa=0 sb=0 sd=0 mult=1 m=1
XMbe Vnode Vb VN GND sky130_fd_pr__nfet_01v8 L=0.5 W=1.5 nf=1 ad='int((nf+1)/2) * W/nf * 0.29' as='int((nf+2)/2) * W/nf * 0.29'
+ pd='2*int((nf+1)/2) * (W/nf + 0.29)' ps='2*int((nf+2)/2) * (W/nf + 0.29)' nrd='0.29 / W' nrs='0.29 / W'
+ sa=0 sb=0 sd=0 mult=1 m=1
XMbf Vnode Vb VN GND sky130_fd_pr__nfet_01v8 L=0.5 W=1.5 nf=1 ad='int((nf+1)/2) * W/nf * 0.29' as='int((nf+2)/2) * W/nf * 0.29'
+ pd='2*int((nf+1)/2) * (W/nf + 0.29)' ps='2*int((nf+2)/2) * (W/nf + 0.29)' nrd='0.29 / W' nrs='0.29 / W'
+ sa=0 sb=0 sd=0 mult=1 m=1
XMbg Vnode Vb VN GND sky130_fd_pr__nfet_01v8 L=0.5 W=1.5 nf=1 ad='int((nf+1)/2) * W/nf * 0.29' as='int((nf+2)/2) * W/nf * 0.29'
+ pd='2*int((nf+1)/2) * (W/nf + 0.29)' ps='2*int((nf+2)/2) * (W/nf + 0.29)' nrd='0.29 / W' nrs='0.29 / W'
+ sa=0 sb=0 sd=0 mult=1 m=1
XMbh Vnode Vb VN GND sky130_fd_pr__nfet_01v8 L=0.5 W=1.5 nf=1 ad='int((nf+1)/2) * W/nf * 0.29' as='int((nf+2)/2) * W/nf * 0.29'
+ pd='2*int((nf+1)/2) * (W/nf + 0.29)' ps='2*int((nf+2)/2) * (W/nf + 0.29)' nrd='0.29 / W' nrs='0.29 / W'
+ sa=0 sb=0 sd=0 mult=1 m=1
XM7a net2 Vcn net1 GND sky130_fd_pr__nfet_01v8 L=0.5 W=3 nf=1 ad='int((nf+1)/2) * W/nf * 0.29' as='int((nf+2)/2) * W/nf * 0.29'
+ pd='2*int((nf+1)/2) * (W/nf + 0.29)' ps='2*int((nf+2)/2) * (W/nf + 0.29)' nrd='0.29 / W' nrs='0.29 / W'
+ sa=0 sb=0 sd=0 mult=1 m=1
XM7b net2 Vcn net1 GND sky130_fd_pr__nfet_01v8 L=0.5 W=3 nf=1 ad='int((nf+1)/2) * W/nf * 0.29' as='int((nf+2)/2) * W/nf * 0.29'
+ pd='2*int((nf+1)/2) * (W/nf + 0.29)' ps='2*int((nf+2)/2) * (W/nf + 0.29)' nrd='0.29 / W' nrs='0.29 / W'
+ sa=0 sb=0 sd=0 mult=1 m=1
XM7c net2 Vcn net1 GND sky130_fd_pr__nfet_01v8 L=0.5 W=3 nf=1 ad='int((nf+1)/2) * W/nf * 0.29' as='int((nf+2)/2) * W/nf * 0.29'
+ pd='2*int((nf+1)/2) * (W/nf + 0.29)' ps='2*int((nf+2)/2) * (W/nf + 0.29)' nrd='0.29 / W' nrs='0.29 / W'
+ sa=0 sb=0 sd=0 mult=1 m=1
XM7d net2 Vcn net1 GND sky130_fd_pr__nfet_01v8 L=0.5 W=3 nf=1 ad='int((nf+1)/2) * W/nf * 0.29' as='int((nf+2)/2) * W/nf * 0.29'
+ pd='2*int((nf+1)/2) * (W/nf + 0.29)' ps='2*int((nf+2)/2) * (W/nf + 0.29)' nrd='0.29 / W' nrs='0.29 / W'
+ sa=0 sb=0 sd=0 mult=1 m=1
XM8a net3 Vcn Vout GND sky130_fd_pr__nfet_01v8 L=0.5 W=3 nf=1 ad='int((nf+1)/2) * W/nf * 0.29' as='int((nf+2)/2) * W/nf * 0.29'
+ pd='2*int((nf+1)/2) * (W/nf + 0.29)' ps='2*int((nf+2)/2) * (W/nf + 0.29)' nrd='0.29 / W' nrs='0.29 / W'
+ sa=0 sb=0 sd=0 mult=1 m=1
XM8b net3 Vcn Vout GND sky130_fd_pr__nfet_01v8 L=0.5 W=3 nf=1 ad='int((nf+1)/2) * W/nf * 0.29' as='int((nf+2)/2) * W/nf * 0.29'
+ pd='2*int((nf+1)/2) * (W/nf + 0.29)' ps='2*int((nf+2)/2) * (W/nf + 0.29)' nrd='0.29 / W' nrs='0.29 / W'
+ sa=0 sb=0 sd=0 mult=1 m=1
XM8c net3 Vcn Vout GND sky130_fd_pr__nfet_01v8 L=0.5 W=3 nf=1 ad='int((nf+1)/2) * W/nf * 0.29' as='int((nf+2)/2) * W/nf * 0.29'
+ pd='2*int((nf+1)/2) * (W/nf + 0.29)' ps='2*int((nf+2)/2) * (W/nf + 0.29)' nrd='0.29 / W' nrs='0.29 / W'
+ sa=0 sb=0 sd=0 mult=1 m=1
XM8d net3 Vcn Vout GND sky130_fd_pr__nfet_01v8 L=0.5 W=3 nf=1 ad='int((nf+1)/2) * W/nf * 0.29' as='int((nf+2)/2) * W/nf * 0.29'
+ pd='2*int((nf+1)/2) * (W/nf + 0.29)' ps='2*int((nf+2)/2) * (W/nf + 0.29)' nrd='0.29 / W' nrs='0.29 / W'
+ sa=0 sb=0 sd=0 mult=1 m=1
XM9a net1 net2 VN GND sky130_fd_pr__nfet_01v8 L=0.5 W=3 nf=1 ad='int((nf+1)/2) * W/nf * 0.29' as='int((nf+2)/2) * W/nf * 0.29'
+ pd='2*int((nf+1)/2) * (W/nf + 0.29)' ps='2*int((nf+2)/2) * (W/nf + 0.29)' nrd='0.29 / W' nrs='0.29 / W'
+ sa=0 sb=0 sd=0 mult=1 m=1
XM9b net1 net2 VN GND sky130_fd_pr__nfet_01v8 L=0.5 W=3 nf=1 ad='int((nf+1)/2) * W/nf * 0.29' as='int((nf+2)/2) * W/nf * 0.29'
+ pd='2*int((nf+1)/2) * (W/nf + 0.29)' ps='2*int((nf+2)/2) * (W/nf + 0.29)' nrd='0.29 / W' nrs='0.29 / W'
+ sa=0 sb=0 sd=0 mult=1 m=1
XM9c net1 net2 VN GND sky130_fd_pr__nfet_01v8 L=0.5 W=3 nf=1 ad='int((nf+1)/2) * W/nf * 0.29' as='int((nf+2)/2) * W/nf * 0.29'
+ pd='2*int((nf+1)/2) * (W/nf + 0.29)' ps='2*int((nf+2)/2) * (W/nf + 0.29)' nrd='0.29 / W' nrs='0.29 / W'
+ sa=0 sb=0 sd=0 mult=1 m=1
XM9d net1 net2 VN GND sky130_fd_pr__nfet_01v8 L=0.5 W=3 nf=1 ad='int((nf+1)/2) * W/nf * 0.29' as='int((nf+2)/2) * W/nf * 0.29'
+ pd='2*int((nf+1)/2) * (W/nf + 0.29)' ps='2*int((nf+2)/2) * (W/nf + 0.29)' nrd='0.29 / W' nrs='0.29 / W'
+ sa=0 sb=0 sd=0 mult=1 m=1
XM10a VN net2 net3 GND sky130_fd_pr__nfet_01v8 L=0.5 W=3 nf=1 ad='int((nf+1)/2) * W/nf * 0.29' as='int((nf+2)/2) * W/nf * 0.29'
+ pd='2*int((nf+1)/2) * (W/nf + 0.29)' ps='2*int((nf+2)/2) * (W/nf + 0.29)' nrd='0.29 / W' nrs='0.29 / W'
+ sa=0 sb=0 sd=0 mult=1 m=1
XM10b VN net2 net3 GND sky130_fd_pr__nfet_01v8 L=0.5 W=3 nf=1 ad='int((nf+1)/2) * W/nf * 0.29' as='int((nf+2)/2) * W/nf * 0.29'
+ pd='2*int((nf+1)/2) * (W/nf + 0.29)' ps='2*int((nf+2)/2) * (W/nf + 0.29)' nrd='0.29 / W' nrs='0.29 / W'
+ sa=0 sb=0 sd=0 mult=1 m=1
XM10c VN net2 net3 GND sky130_fd_pr__nfet_01v8 L=0.5 W=3 nf=1 ad='int((nf+1)/2) * W/nf * 0.29' as='int((nf+2)/2) * W/nf * 0.29'
+ pd='2*int((nf+1)/2) * (W/nf + 0.29)' ps='2*int((nf+2)/2) * (W/nf + 0.29)' nrd='0.29 / W' nrs='0.29 / W'
+ sa=0 sb=0 sd=0 mult=1 m=1
XM1 VN net2 net3 GND sky130_fd_pr__nfet_01v8 L=0.5 W=3 nf=1 ad='int((nf+1)/2) * W/nf * 0.29' as='int((nf+2)/2) * W/nf * 0.29'
+ pd='2*int((nf+1)/2) * (W/nf + 0.29)' ps='2*int((nf+2)/2) * (W/nf + 0.29)' nrd='0.29 / W' nrs='0.29 / W'
+ sa=0 sb=0 sd=0 mult=1 m=1
XM5a net2 Vcp M1top VDD sky130_fd_pr__pfet_01v8 L=0.5 W=8 nf=1 ad='int((nf+1)/2) * W/nf * 0.29' as='int((nf+2)/2) * W/nf * 0.29'
+ pd='2*int((nf+1)/2) * (W/nf + 0.29)' ps='2*int((nf+2)/2) * (W/nf + 0.29)' nrd='0.29 / W' nrs='0.29 / W'
+ sa=0 sb=0 sd=0 mult=1 m=1
XM5b net2 Vcp M1top VDD sky130_fd_pr__pfet_01v8 L=0.5 W=8 nf=1 ad='int((nf+1)/2) * W/nf * 0.29' as='int((nf+2)/2) * W/nf * 0.29'
+ pd='2*int((nf+1)/2) * (W/nf + 0.29)' ps='2*int((nf+2)/2) * (W/nf + 0.29)' nrd='0.29 / W' nrs='0.29 / W'
+ sa=0 sb=0 sd=0 mult=1 m=1
XM5c net2 Vcp M1top VDD sky130_fd_pr__pfet_01v8 L=0.5 W=8 nf=1 ad='int((nf+1)/2) * W/nf * 0.29' as='int((nf+2)/2) * W/nf * 0.29'
+ pd='2*int((nf+1)/2) * (W/nf + 0.29)' ps='2*int((nf+2)/2) * (W/nf + 0.29)' nrd='0.29 / W' nrs='0.29 / W'
+ sa=0 sb=0 sd=0 mult=1 m=1
XM5d net2 Vcp M1top VDD sky130_fd_pr__pfet_01v8 L=0.5 W=8 nf=1 ad='int((nf+1)/2) * W/nf * 0.29' as='int((nf+2)/2) * W/nf * 0.29'
+ pd='2*int((nf+1)/2) * (W/nf + 0.29)' ps='2*int((nf+2)/2) * (W/nf + 0.29)' nrd='0.29 / W' nrs='0.29 / W'
+ sa=0 sb=0 sd=0 mult=1 m=1
XM6a Vout Vcp M2top VDD sky130_fd_pr__pfet_01v8 L=0.5 W=8 nf=1 ad='int((nf+1)/2) * W/nf * 0.29' as='int((nf+2)/2) * W/nf * 0.29'
+ pd='2*int((nf+1)/2) * (W/nf + 0.29)' ps='2*int((nf+2)/2) * (W/nf + 0.29)' nrd='0.29 / W' nrs='0.29 / W'
+ sa=0 sb=0 sd=0 mult=1 m=1
XM6b Vout Vcp M2top VDD sky130_fd_pr__pfet_01v8 L=0.5 W=8 nf=1 ad='int((nf+1)/2) * W/nf * 0.29' as='int((nf+2)/2) * W/nf * 0.29'
+ pd='2*int((nf+1)/2) * (W/nf + 0.29)' ps='2*int((nf+2)/2) * (W/nf + 0.29)' nrd='0.29 / W' nrs='0.29 / W'
+ sa=0 sb=0 sd=0 mult=1 m=1
XM6c Vout Vcp M2top VDD sky130_fd_pr__pfet_01v8 L=0.5 W=8 nf=1 ad='int((nf+1)/2) * W/nf * 0.29' as='int((nf+2)/2) * W/nf * 0.29'
+ pd='2*int((nf+1)/2) * (W/nf + 0.29)' ps='2*int((nf+2)/2) * (W/nf + 0.29)' nrd='0.29 / W' nrs='0.29 / W'
+ sa=0 sb=0 sd=0 mult=1 m=1
XM6d Vout Vcp M2top VDD sky130_fd_pr__pfet_01v8 L=0.5 W=8 nf=1 ad='int((nf+1)/2) * W/nf * 0.29' as='int((nf+2)/2) * W/nf * 0.29'
+ pd='2*int((nf+1)/2) * (W/nf + 0.29)' ps='2*int((nf+2)/2) * (W/nf + 0.29)' nrd='0.29 / W' nrs='0.29 / W'
+ sa=0 sb=0 sd=0 mult=1 m=1
XM3a M1top Vbp VP VDD sky130_fd_pr__pfet_01v8 L=0.5 W=8 nf=1 ad='int((nf+1)/2) * W/nf * 0.29' as='int((nf+2)/2) * W/nf * 0.29'
+ pd='2*int((nf+1)/2) * (W/nf + 0.29)' ps='2*int((nf+2)/2) * (W/nf + 0.29)' nrd='0.29 / W' nrs='0.29 / W'
+ sa=0 sb=0 sd=0 mult=1 m=1
XM3b M1top Vbp VP VDD sky130_fd_pr__pfet_01v8 L=0.5 W=8 nf=1 ad='int((nf+1)/2) * W/nf * 0.29' as='int((nf+2)/2) * W/nf * 0.29'
+ pd='2*int((nf+1)/2) * (W/nf + 0.29)' ps='2*int((nf+2)/2) * (W/nf + 0.29)' nrd='0.29 / W' nrs='0.29 / W'
+ sa=0 sb=0 sd=0 mult=1 m=1
XM3c M1top Vbp VP VDD sky130_fd_pr__pfet_01v8 L=0.5 W=8 nf=1 ad='int((nf+1)/2) * W/nf * 0.29' as='int((nf+2)/2) * W/nf * 0.29'
+ pd='2*int((nf+1)/2) * (W/nf + 0.29)' ps='2*int((nf+2)/2) * (W/nf + 0.29)' nrd='0.29 / W' nrs='0.29 / W'
+ sa=0 sb=0 sd=0 mult=1 m=1
XM3d M1top Vbp VP VDD sky130_fd_pr__pfet_01v8 L=0.5 W=8 nf=1 ad='int((nf+1)/2) * W/nf * 0.29' as='int((nf+2)/2) * W/nf * 0.29'
+ pd='2*int((nf+1)/2) * (W/nf + 0.29)' ps='2*int((nf+2)/2) * (W/nf + 0.29)' nrd='0.29 / W' nrs='0.29 / W'
+ sa=0 sb=0 sd=0 mult=1 m=1
XM4a M2top Vbp VP VDD sky130_fd_pr__pfet_01v8 L=0.5 W=8 nf=1 ad='int((nf+1)/2) * W/nf * 0.29' as='int((nf+2)/2) * W/nf * 0.29'
+ pd='2*int((nf+1)/2) * (W/nf + 0.29)' ps='2*int((nf+2)/2) * (W/nf + 0.29)' nrd='0.29 / W' nrs='0.29 / W'
+ sa=0 sb=0 sd=0 mult=1 m=1
XM4b M2top Vbp VP VDD sky130_fd_pr__pfet_01v8 L=0.5 W=8 nf=1 ad='int((nf+1)/2) * W/nf * 0.29' as='int((nf+2)/2) * W/nf * 0.29'
+ pd='2*int((nf+1)/2) * (W/nf + 0.29)' ps='2*int((nf+2)/2) * (W/nf + 0.29)' nrd='0.29 / W' nrs='0.29 / W'
+ sa=0 sb=0 sd=0 mult=1 m=1
XM4c M2top Vbp VP VDD sky130_fd_pr__pfet_01v8 L=0.5 W=8 nf=1 ad='int((nf+1)/2) * W/nf * 0.29' as='int((nf+2)/2) * W/nf * 0.29'
+ pd='2*int((nf+1)/2) * (W/nf + 0.29)' ps='2*int((nf+2)/2) * (W/nf + 0.29)' nrd='0.29 / W' nrs='0.29 / W'
+ sa=0 sb=0 sd=0 mult=1 m=1
XM4d M2top Vbp VP VDD sky130_fd_pr__pfet_01v8 L=0.5 W=8 nf=1 ad='int((nf+1)/2) * W/nf * 0.29' as='int((nf+2)/2) * W/nf * 0.29'
+ pd='2*int((nf+1)/2) * (W/nf + 0.29)' ps='2*int((nf+2)/2) * (W/nf + 0.29)' nrd='0.29 / W' nrs='0.29 / W'
+ sa=0 sb=0 sd=0 mult=1 m=1
.ends


* expanding   symbol:  /home/madvlsi/dev/git/magic-dds/xschem/other_project_files/inverter.sym # of
*+ pins=4
** sym_path: xschem/other_project_files/inverter.sym
** sch_path: xschem/other_project_files/inverter.sch
.subckt inverter VP A Y VN
*.iopin VP
*.iopin VN
*.ipin A
*.opin Y
XM1 Y A VN VN sky130_fd_pr__nfet_01v8 L=0.15 W=1 nf=1 ad='int((nf+1)/2) * W/nf * 0.29' as='int((nf+2)/2) * W/nf * 0.29'
+ pd='2*int((nf+1)/2) * (W/nf + 0.29)' ps='2*int((nf+2)/2) * (W/nf + 0.29)' nrd='0.29 / W' nrs='0.29 / W'
+ sa=0 sb=0 sd=0 mult=1 m=1
XM2 Y A VP VP sky130_fd_pr__pfet_01v8 L=0.15 W=4 nf=1 ad='int((nf+1)/2) * W/nf * 0.29' as='int((nf+2)/2) * W/nf * 0.29'
+ pd='2*int((nf+1)/2) * (W/nf + 0.29)' ps='2*int((nf+2)/2) * (W/nf + 0.29)' nrd='0.29 / W' nrs='0.29 / W'
+ sa=0 sb=0 sd=0 mult=1 m=1
.ends

.GLOBAL VDD
.GLOBAL GND
.end
